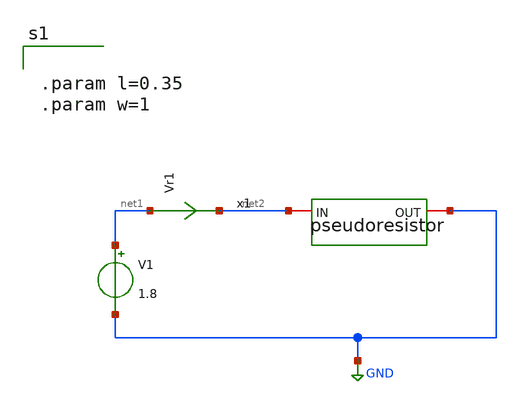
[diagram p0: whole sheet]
** sch_path: pseudoresistor_tb.sch
**.subckt pseudoresistor_tb
x1 net2 GND pseudoresistor
V1 net1 GND 1.8
.save i(v1)
Vr1 net1 net2 0
.save i(vr1)
**** begin user architecture code

** opencircuitdesign pdks install
.lib $::SKYWATER_MODELS/sky130.lib.spice tt
.include $::SKYWATER_STDCELLS/sky130_fd_sc_hd.spice

.control
	dc V1 0 1 0.0001
	plot i(V1)
.endc
.save all


** opencircuitdesign pdks install
.lib $::SKYWATER_MODELS/sky130.lib.spice tt
.include $::SKYWATER_STDCELLS/sky130_fd_sc_hd.spice

.control

	dc V2 0 1 0.0001
	plot i(V2)


.endc
.save all



.param l=0.35
.param w=1



**** end user architecture code
**.ends

* expanding   symbol:  pseudoresistor.sym # of pins=2
** sym_path: pseudoresistor.sym
** sch_path: pseudoresistor.sch
.subckt pseudoresistor IN OUT
*.iopin IN
*.iopin OUT
XM5 net1 IN IN IN sky130_fd_pr__pfet_01v8 L=0.5 W=1 nf=1 ad='int((nf+1)/2) * W/nf * 0.29' as='int((nf+2)/2) * W/nf * 0.29'
+ pd='2*int((nf+1)/2) * (W/nf + 0.29)' ps='2*int((nf+2)/2) * (W/nf + 0.29)' nrd='0.29 / W' nrs='0.29 / W'
+ sa=0 sb=0 sd=0 mult=10 m=10
XM1 net2 net2 net1 net2 sky130_fd_pr__pfet_01v8 L=0.5 W=1 nf=1 ad='int((nf+1)/2) * W/nf * 0.29' as='int((nf+2)/2) * W/nf * 0.29'
+ pd='2*int((nf+1)/2) * (W/nf + 0.29)' ps='2*int((nf+2)/2) * (W/nf + 0.29)' nrd='0.29 / W' nrs='0.29 / W'
+ sa=0 sb=0 sd=0 mult=10 m=10
XM2 net3 net2 net2 net2 sky130_fd_pr__pfet_01v8 L=0.5 W=1 nf=1 ad='int((nf+1)/2) * W/nf * 0.29' as='int((nf+2)/2) * W/nf * 0.29'
+ pd='2*int((nf+1)/2) * (W/nf + 0.29)' ps='2*int((nf+2)/2) * (W/nf + 0.29)' nrd='0.29 / W' nrs='0.29 / W'
+ sa=0 sb=0 sd=0 mult=10 m=10
XM3 OUT OUT net3 OUT sky130_fd_pr__pfet_01v8 L=0.5 W=1.2 nf=1 ad='int((nf+1)/2) * W/nf * 0.29' as='int((nf+2)/2) * W/nf * 0.29'
+ pd='2*int((nf+1)/2) * (W/nf + 0.29)' ps='2*int((nf+2)/2) * (W/nf + 0.29)' nrd='0.29 / W' nrs='0.29 / W'
+ sa=0 sb=0 sd=0 mult=1 m=1
.ends

.GLOBAL GND
.end
